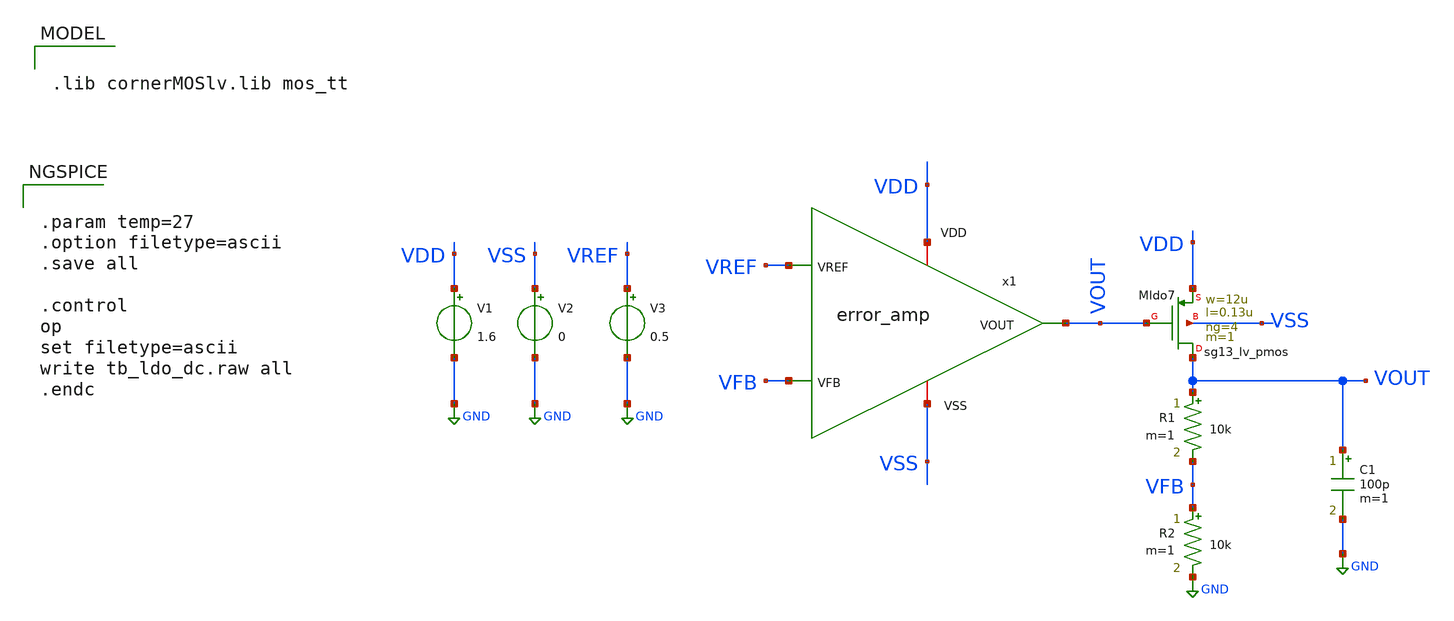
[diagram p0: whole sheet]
** sch_path: analog/tb/tb_error_amp.sch
**.subckt tb_error_amp
XMldo7 VOUT VOUT VDD VSS sg13_lv_pmos w=12u l=0.13u ng=4 m=1 mm_ok=1
V1 VDD GND 1.6
R1 VOUT VFB 10k m=1
V2 VSS GND 0
V3 VREF GND 0.5
R2 VFB GND 10k m=1
C1 VOUT GND 100p m=1
x1 VDD VOUT VREF VFB VSS error_amp
**** begin user architecture code


.param temp=27
.option filetype=ascii
.save all

.control
op
set filetype=ascii
write tb_ldo_dc.raw all
.endc



.lib cornerMOSlv.lib mos_tt

**** end user architecture code
**.ends

* expanding   symbol:  error_amp.sym # of pins=5
** sym_path: analog/core/error_amp.sym
** sch_path: analog/core/error_amp.sch
.subckt error_amp VDD VOUT VREF VFB VSS
*.ipin VREF
*.iopin VDD
*.opin VOUT
*.ipin VFB
*.iopin VSS
XMldo1 net1 VFB net2 VSS sg13_lv_nmos w=1.2u l=0.13u ng=1 m=1 mm_ok=1
XMldo4 VOUT net1 VDD VDD sg13_lv_pmos w=2.4u l=0.13u ng=1 m=1 mm_ok=1
XMldo2 VOUT VREF net2 VSS sg13_lv_nmos w=1.2u l=0.13u ng=1 m=1 mm_ok=1
XMldo3 net1 net1 VDD VDD sg13_lv_pmos w=2.4u l=0.13u ng=1 m=1 mm_ok=1
XMldo5 net2 net3 VSS VSS sg13_lv_nmos w=2u l=0.13u ng=1 m=1 mm_ok=1
XMldo6 net3 net3 VSS VSS sg13_lv_nmos w=1u l=0.13u ng=1 m=1 mm_ok=1
I0 VDD net3 2u
.ends

.GLOBAL GND
.end
